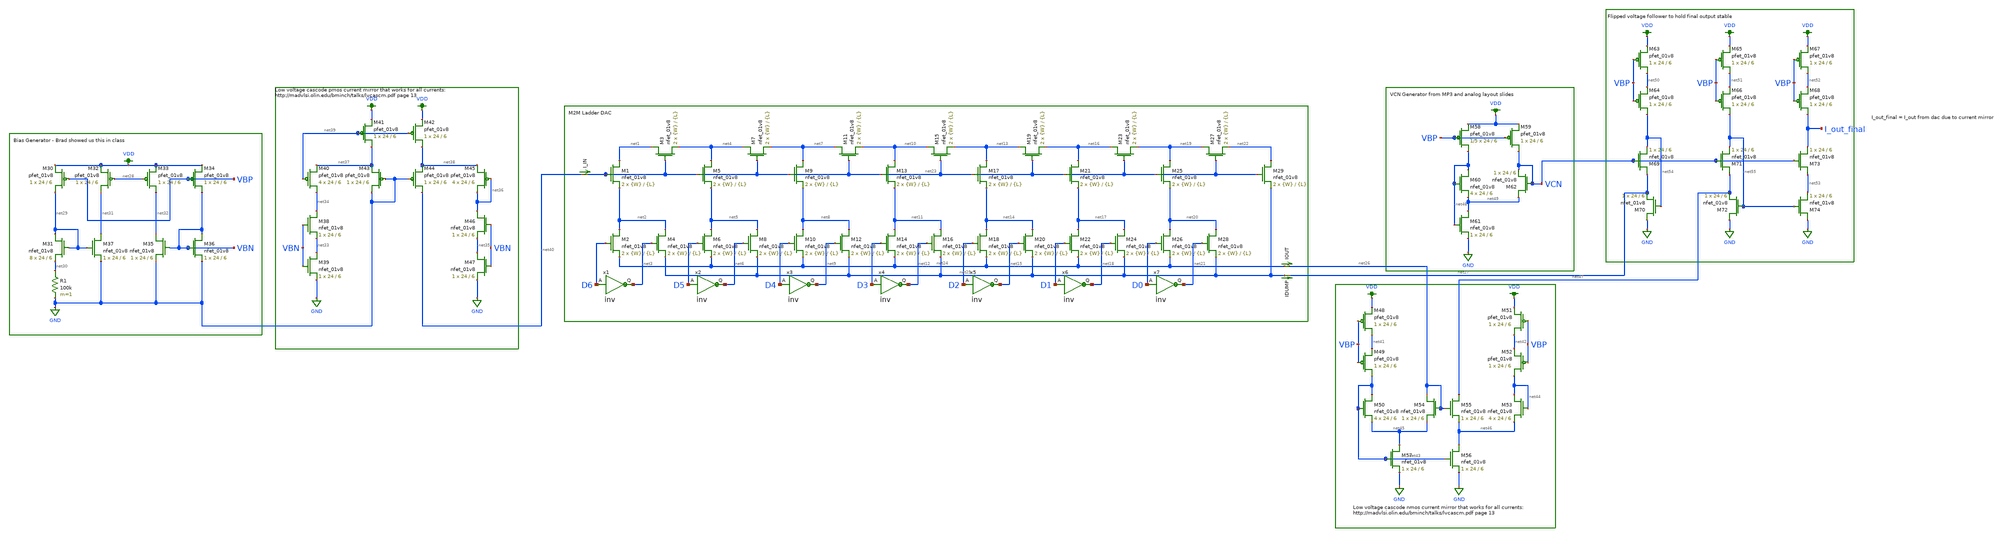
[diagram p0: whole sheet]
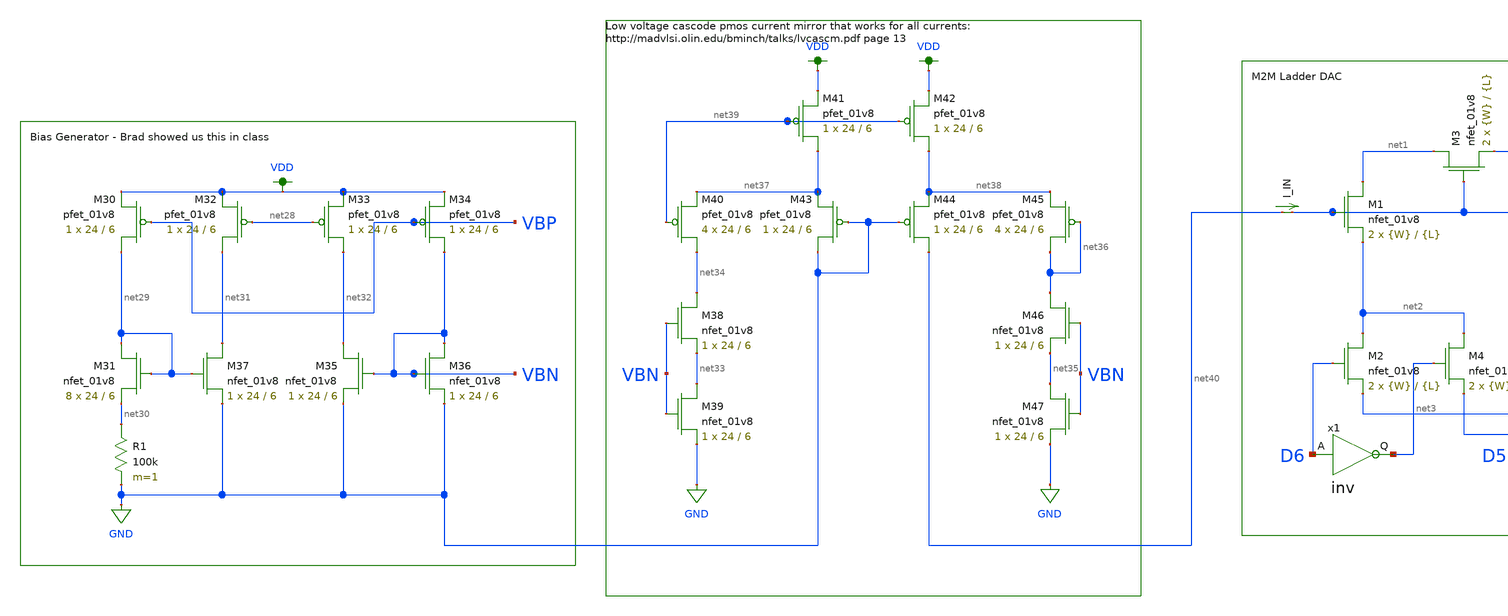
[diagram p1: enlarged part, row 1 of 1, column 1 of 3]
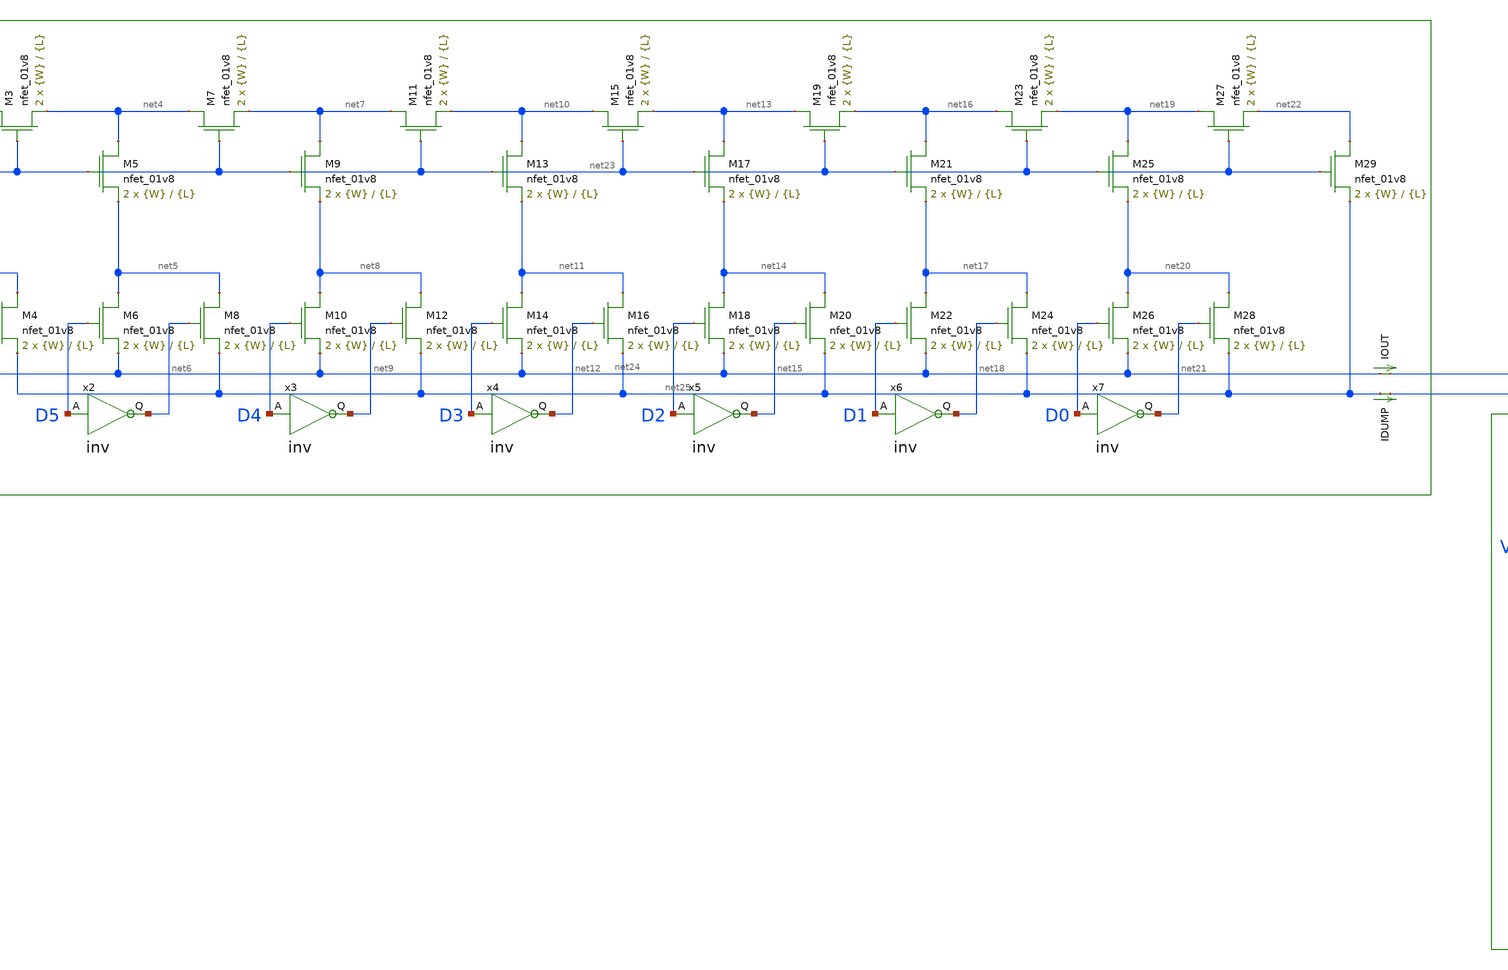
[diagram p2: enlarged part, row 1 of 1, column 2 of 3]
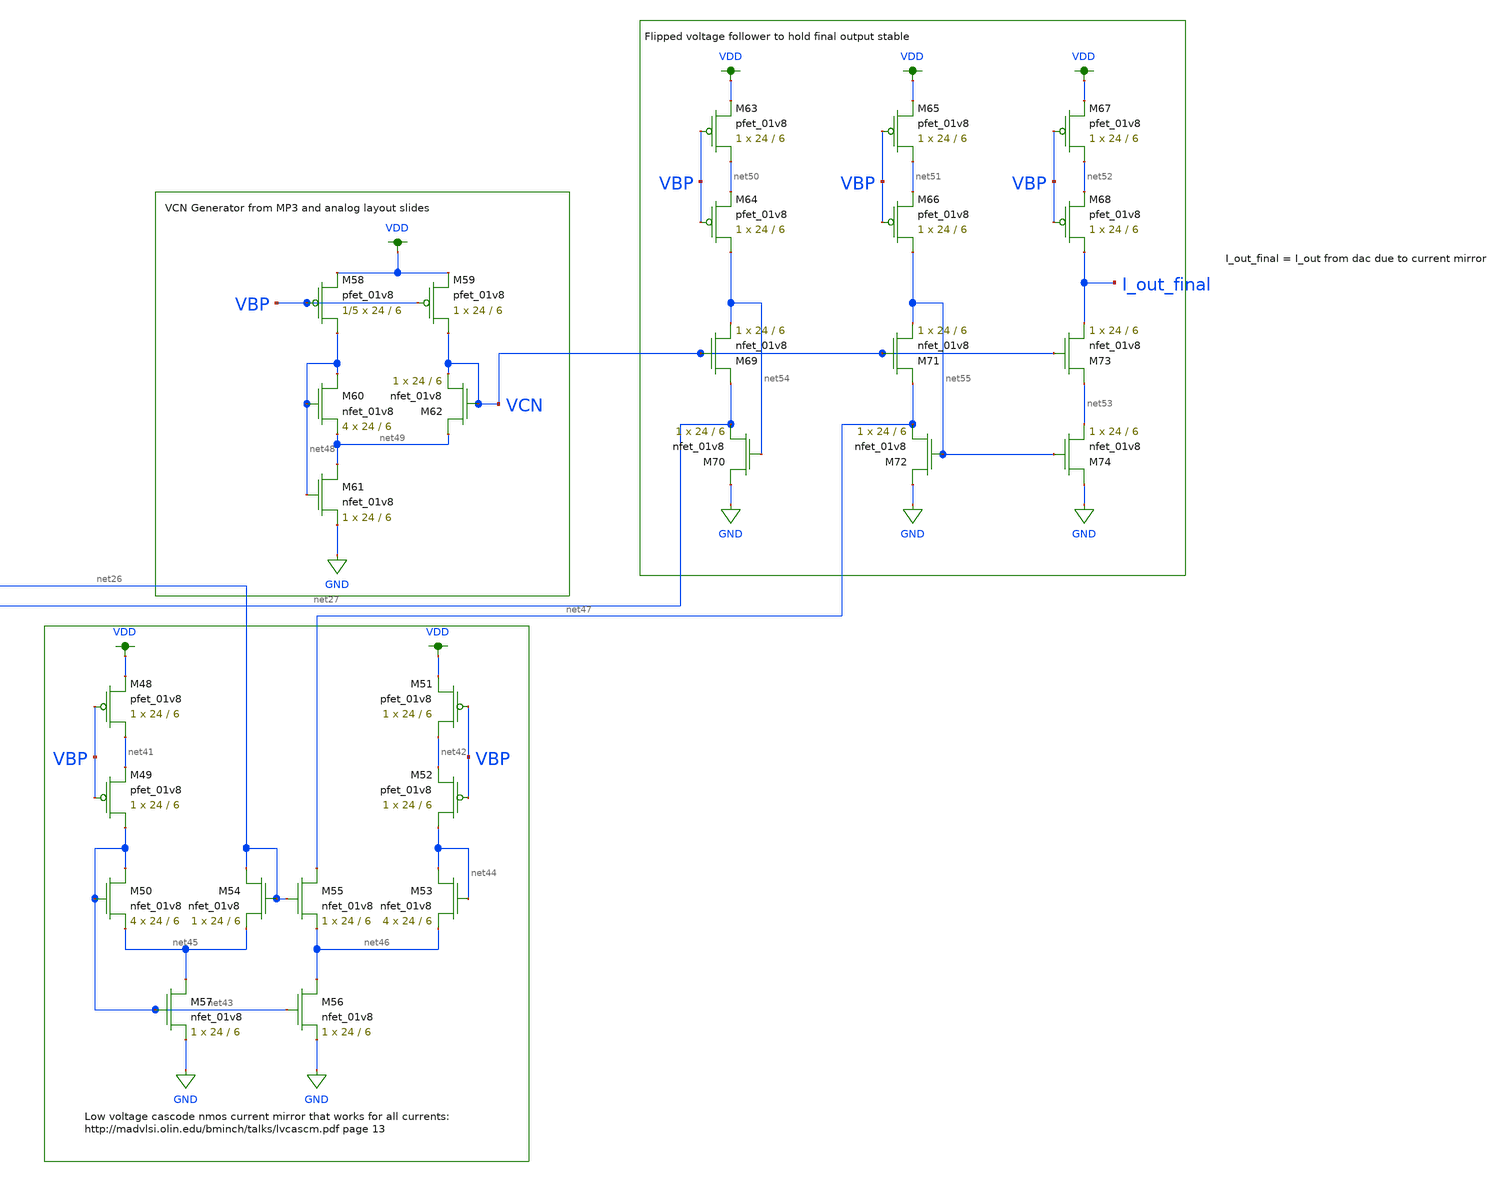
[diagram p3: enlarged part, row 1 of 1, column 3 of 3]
** sch_path: top_dac7.sch
**.subckt top_dac7
XM1 net1 net23 net2 GND sky130_fd_pr__nfet_01v8 L={L} W={W} nf=1 ad='int((nf+1)/2) * W/nf * 0.29' as='int((nf+2)/2) * W/nf * 0.29'
+ pd='2*int((nf+1)/2) * (W/nf + 0.29)' ps='2*int((nf+2)/2) * (W/nf + 0.29)' nrd='0.29 / W' nrs='0.29 / W'
+ sa=0 sb=0 sd=0 mult=2 m=2
IOUT net24 net26 0
.save i(iout)
XM2 net2 D6 net24 GND sky130_fd_pr__nfet_01v8 L={L} W={W} nf=1 ad='int((nf+1)/2) * W/nf * 0.29' as='int((nf+2)/2) * W/nf * 0.29'
+ pd='2*int((nf+1)/2) * (W/nf + 0.29)' ps='2*int((nf+2)/2) * (W/nf + 0.29)' nrd='0.29 / W' nrs='0.29 / W'
+ sa=0 sb=0 sd=0 mult=2 m=2
XM3 net1 net23 net4 GND sky130_fd_pr__nfet_01v8 L={L} W={W} nf=1 ad='int((nf+1)/2) * W/nf * 0.29' as='int((nf+2)/2) * W/nf * 0.29'
+ pd='2*int((nf+1)/2) * (W/nf + 0.29)' ps='2*int((nf+2)/2) * (W/nf + 0.29)' nrd='0.29 / W' nrs='0.29 / W'
+ sa=0 sb=0 sd=0 mult=2 m=2
XM4 net2 net3 net25 GND sky130_fd_pr__nfet_01v8 L={L} W={W} nf=1 ad='int((nf+1)/2) * W/nf * 0.29' as='int((nf+2)/2) * W/nf * 0.29'
+ pd='2*int((nf+1)/2) * (W/nf + 0.29)' ps='2*int((nf+2)/2) * (W/nf + 0.29)' nrd='0.29 / W' nrs='0.29 / W'
+ sa=0 sb=0 sd=0 mult=2 m=2
XM5 net4 net23 net5 GND sky130_fd_pr__nfet_01v8 L={L} W={W} nf=1 ad='int((nf+1)/2) * W/nf * 0.29' as='int((nf+2)/2) * W/nf * 0.29'
+ pd='2*int((nf+1)/2) * (W/nf + 0.29)' ps='2*int((nf+2)/2) * (W/nf + 0.29)' nrd='0.29 / W' nrs='0.29 / W'
+ sa=0 sb=0 sd=0 mult=2 m=2
XM6 net5 D5 net24 GND sky130_fd_pr__nfet_01v8 L={L} W={W} nf=1 ad='int((nf+1)/2) * W/nf * 0.29' as='int((nf+2)/2) * W/nf * 0.29'
+ pd='2*int((nf+1)/2) * (W/nf + 0.29)' ps='2*int((nf+2)/2) * (W/nf + 0.29)' nrd='0.29 / W' nrs='0.29 / W'
+ sa=0 sb=0 sd=0 mult=2 m=2
XM7 net4 net23 net7 GND sky130_fd_pr__nfet_01v8 L={L} W={W} nf=1 ad='int((nf+1)/2) * W/nf * 0.29' as='int((nf+2)/2) * W/nf * 0.29'
+ pd='2*int((nf+1)/2) * (W/nf + 0.29)' ps='2*int((nf+2)/2) * (W/nf + 0.29)' nrd='0.29 / W' nrs='0.29 / W'
+ sa=0 sb=0 sd=0 mult=2 m=2
XM8 net5 net6 net25 GND sky130_fd_pr__nfet_01v8 L={L} W={W} nf=1 ad='int((nf+1)/2) * W/nf * 0.29' as='int((nf+2)/2) * W/nf * 0.29'
+ pd='2*int((nf+1)/2) * (W/nf + 0.29)' ps='2*int((nf+2)/2) * (W/nf + 0.29)' nrd='0.29 / W' nrs='0.29 / W'
+ sa=0 sb=0 sd=0 mult=2 m=2
XM9 net7 net23 net8 GND sky130_fd_pr__nfet_01v8 L={L} W={W} nf=1 ad='int((nf+1)/2) * W/nf * 0.29' as='int((nf+2)/2) * W/nf * 0.29'
+ pd='2*int((nf+1)/2) * (W/nf + 0.29)' ps='2*int((nf+2)/2) * (W/nf + 0.29)' nrd='0.29 / W' nrs='0.29 / W'
+ sa=0 sb=0 sd=0 mult=2 m=2
XM10 net8 D4 net24 GND sky130_fd_pr__nfet_01v8 L={L} W={W} nf=1 ad='int((nf+1)/2) * W/nf * 0.29' as='int((nf+2)/2) * W/nf * 0.29'
+ pd='2*int((nf+1)/2) * (W/nf + 0.29)' ps='2*int((nf+2)/2) * (W/nf + 0.29)' nrd='0.29 / W' nrs='0.29 / W'
+ sa=0 sb=0 sd=0 mult=2 m=2
XM11 net7 net23 net10 GND sky130_fd_pr__nfet_01v8 L={L} W={W} nf=1 ad='int((nf+1)/2) * W/nf * 0.29' as='int((nf+2)/2) * W/nf * 0.29'
+ pd='2*int((nf+1)/2) * (W/nf + 0.29)' ps='2*int((nf+2)/2) * (W/nf + 0.29)' nrd='0.29 / W' nrs='0.29 / W'
+ sa=0 sb=0 sd=0 mult=2 m=2
XM12 net8 net9 net25 GND sky130_fd_pr__nfet_01v8 L={L} W={W} nf=1 ad='int((nf+1)/2) * W/nf * 0.29' as='int((nf+2)/2) * W/nf * 0.29'
+ pd='2*int((nf+1)/2) * (W/nf + 0.29)' ps='2*int((nf+2)/2) * (W/nf + 0.29)' nrd='0.29 / W' nrs='0.29 / W'
+ sa=0 sb=0 sd=0 mult=2 m=2
XM13 net10 net23 net11 GND sky130_fd_pr__nfet_01v8 L={L} W={W} nf=1 ad='int((nf+1)/2) * W/nf * 0.29'
+ as='int((nf+2)/2) * W/nf * 0.29' pd='2*int((nf+1)/2) * (W/nf + 0.29)' ps='2*int((nf+2)/2) * (W/nf + 0.29)'
+ nrd='0.29 / W' nrs='0.29 / W' sa=0 sb=0 sd=0 mult=2 m=2
XM14 net11 D3 net24 GND sky130_fd_pr__nfet_01v8 L={L} W={W} nf=1 ad='int((nf+1)/2) * W/nf * 0.29' as='int((nf+2)/2) * W/nf * 0.29'
+ pd='2*int((nf+1)/2) * (W/nf + 0.29)' ps='2*int((nf+2)/2) * (W/nf + 0.29)' nrd='0.29 / W' nrs='0.29 / W'
+ sa=0 sb=0 sd=0 mult=2 m=2
XM15 net10 net23 net13 GND sky130_fd_pr__nfet_01v8 L={L} W={W} nf=1 ad='int((nf+1)/2) * W/nf * 0.29'
+ as='int((nf+2)/2) * W/nf * 0.29' pd='2*int((nf+1)/2) * (W/nf + 0.29)' ps='2*int((nf+2)/2) * (W/nf + 0.29)'
+ nrd='0.29 / W' nrs='0.29 / W' sa=0 sb=0 sd=0 mult=2 m=2
XM16 net11 net12 net25 GND sky130_fd_pr__nfet_01v8 L={L} W={W} nf=1 ad='int((nf+1)/2) * W/nf * 0.29'
+ as='int((nf+2)/2) * W/nf * 0.29' pd='2*int((nf+1)/2) * (W/nf + 0.29)' ps='2*int((nf+2)/2) * (W/nf + 0.29)'
+ nrd='0.29 / W' nrs='0.29 / W' sa=0 sb=0 sd=0 mult=2 m=2
XM17 net13 net23 net14 GND sky130_fd_pr__nfet_01v8 L={L} W={W} nf=1 ad='int((nf+1)/2) * W/nf * 0.29'
+ as='int((nf+2)/2) * W/nf * 0.29' pd='2*int((nf+1)/2) * (W/nf + 0.29)' ps='2*int((nf+2)/2) * (W/nf + 0.29)'
+ nrd='0.29 / W' nrs='0.29 / W' sa=0 sb=0 sd=0 mult=2 m=2
XM18 net14 D2 net24 GND sky130_fd_pr__nfet_01v8 L={L} W={W} nf=1 ad='int((nf+1)/2) * W/nf * 0.29' as='int((nf+2)/2) * W/nf * 0.29'
+ pd='2*int((nf+1)/2) * (W/nf + 0.29)' ps='2*int((nf+2)/2) * (W/nf + 0.29)' nrd='0.29 / W' nrs='0.29 / W'
+ sa=0 sb=0 sd=0 mult=2 m=2
XM19 net13 net23 net16 GND sky130_fd_pr__nfet_01v8 L={L} W={W} nf=1 ad='int((nf+1)/2) * W/nf * 0.29'
+ as='int((nf+2)/2) * W/nf * 0.29' pd='2*int((nf+1)/2) * (W/nf + 0.29)' ps='2*int((nf+2)/2) * (W/nf + 0.29)'
+ nrd='0.29 / W' nrs='0.29 / W' sa=0 sb=0 sd=0 mult=2 m=2
XM20 net14 net15 net25 GND sky130_fd_pr__nfet_01v8 L={L} W={W} nf=1 ad='int((nf+1)/2) * W/nf * 0.29'
+ as='int((nf+2)/2) * W/nf * 0.29' pd='2*int((nf+1)/2) * (W/nf + 0.29)' ps='2*int((nf+2)/2) * (W/nf + 0.29)'
+ nrd='0.29 / W' nrs='0.29 / W' sa=0 sb=0 sd=0 mult=2 m=2
XM21 net16 net23 net17 GND sky130_fd_pr__nfet_01v8 L={L} W={W} nf=1 ad='int((nf+1)/2) * W/nf * 0.29'
+ as='int((nf+2)/2) * W/nf * 0.29' pd='2*int((nf+1)/2) * (W/nf + 0.29)' ps='2*int((nf+2)/2) * (W/nf + 0.29)'
+ nrd='0.29 / W' nrs='0.29 / W' sa=0 sb=0 sd=0 mult=2 m=2
XM22 net17 D1 net24 GND sky130_fd_pr__nfet_01v8 L={L} W={W} nf=1 ad='int((nf+1)/2) * W/nf * 0.29' as='int((nf+2)/2) * W/nf * 0.29'
+ pd='2*int((nf+1)/2) * (W/nf + 0.29)' ps='2*int((nf+2)/2) * (W/nf + 0.29)' nrd='0.29 / W' nrs='0.29 / W'
+ sa=0 sb=0 sd=0 mult=2 m=2
XM23 net16 net23 net19 GND sky130_fd_pr__nfet_01v8 L={L} W={W} nf=1 ad='int((nf+1)/2) * W/nf * 0.29'
+ as='int((nf+2)/2) * W/nf * 0.29' pd='2*int((nf+1)/2) * (W/nf + 0.29)' ps='2*int((nf+2)/2) * (W/nf + 0.29)'
+ nrd='0.29 / W' nrs='0.29 / W' sa=0 sb=0 sd=0 mult=2 m=2
XM24 net17 net18 net25 GND sky130_fd_pr__nfet_01v8 L={L} W={W} nf=1 ad='int((nf+1)/2) * W/nf * 0.29'
+ as='int((nf+2)/2) * W/nf * 0.29' pd='2*int((nf+1)/2) * (W/nf + 0.29)' ps='2*int((nf+2)/2) * (W/nf + 0.29)'
+ nrd='0.29 / W' nrs='0.29 / W' sa=0 sb=0 sd=0 mult=2 m=2
XM25 net19 net23 net20 GND sky130_fd_pr__nfet_01v8 L={L} W={W} nf=1 ad='int((nf+1)/2) * W/nf * 0.29'
+ as='int((nf+2)/2) * W/nf * 0.29' pd='2*int((nf+1)/2) * (W/nf + 0.29)' ps='2*int((nf+2)/2) * (W/nf + 0.29)'
+ nrd='0.29 / W' nrs='0.29 / W' sa=0 sb=0 sd=0 mult=2 m=2
XM26 net20 D0 net24 GND sky130_fd_pr__nfet_01v8 L={L} W={W} nf=1 ad='int((nf+1)/2) * W/nf * 0.29' as='int((nf+2)/2) * W/nf * 0.29'
+ pd='2*int((nf+1)/2) * (W/nf + 0.29)' ps='2*int((nf+2)/2) * (W/nf + 0.29)' nrd='0.29 / W' nrs='0.29 / W'
+ sa=0 sb=0 sd=0 mult=2 m=2
XM27 net19 net23 net22 GND sky130_fd_pr__nfet_01v8 L={L} W={W} nf=1 ad='int((nf+1)/2) * W/nf * 0.29'
+ as='int((nf+2)/2) * W/nf * 0.29' pd='2*int((nf+1)/2) * (W/nf + 0.29)' ps='2*int((nf+2)/2) * (W/nf + 0.29)'
+ nrd='0.29 / W' nrs='0.29 / W' sa=0 sb=0 sd=0 mult=2 m=2
XM28 net20 net21 net25 GND sky130_fd_pr__nfet_01v8 L={L} W={W} nf=1 ad='int((nf+1)/2) * W/nf * 0.29'
+ as='int((nf+2)/2) * W/nf * 0.29' pd='2*int((nf+1)/2) * (W/nf + 0.29)' ps='2*int((nf+2)/2) * (W/nf + 0.29)'
+ nrd='0.29 / W' nrs='0.29 / W' sa=0 sb=0 sd=0 mult=2 m=2
XM29 net22 net23 net25 GND sky130_fd_pr__nfet_01v8 L={L} W={W} nf=1 ad='int((nf+1)/2) * W/nf * 0.29'
+ as='int((nf+2)/2) * W/nf * 0.29' pd='2*int((nf+1)/2) * (W/nf + 0.29)' ps='2*int((nf+2)/2) * (W/nf + 0.29)'
+ nrd='0.29 / W' nrs='0.29 / W' sa=0 sb=0 sd=0 mult=2 m=2
IDUMP net25 net27 0
.save i(idump)
I_IN net40 net23 0
.save i(i_in)
x1 net3 D6 inv
x2 net6 D5 inv
x3 net9 D4 inv
x4 net12 D3 inv
x5 net15 D2 inv
x6 net18 D1 inv
x7 net21 D0 inv
XM30 net29 VBP VDD VDD sky130_fd_pr__pfet_01v8 L=6 W=24 nf=1 ad='int((nf+1)/2) * W/nf * 0.29' as='int((nf+2)/2) * W/nf * 0.29'
+ pd='2*int((nf+1)/2) * (W/nf + 0.29)' ps='2*int((nf+2)/2) * (W/nf + 0.29)' nrd='0.29 / W' nrs='0.29 / W'
+ sa=0 sb=0 sd=0 mult=1 m=1
XM31 net29 net29 net30 GND sky130_fd_pr__nfet_01v8 L=6 W=24 nf=1 ad='int((nf+1)/2) * W/nf * 0.29' as='int((nf+2)/2) * W/nf * 0.29'
+ pd='2*int((nf+1)/2) * (W/nf + 0.29)' ps='2*int((nf+2)/2) * (W/nf + 0.29)' nrd='0.29 / W' nrs='0.29 / W'
+ sa=0 sb=0 sd=0 mult=8 m=8
XM32 net31 net28 VDD VDD sky130_fd_pr__pfet_01v8 L=6 W=24 nf=1 ad='int((nf+1)/2) * W/nf * 0.29' as='int((nf+2)/2) * W/nf * 0.29'
+ pd='2*int((nf+1)/2) * (W/nf + 0.29)' ps='2*int((nf+2)/2) * (W/nf + 0.29)' nrd='0.29 / W' nrs='0.29 / W'
+ sa=0 sb=0 sd=0 mult=1 m=1
XM33 net32 net28 VDD VDD sky130_fd_pr__pfet_01v8 L=6 W=24 nf=1 ad='int((nf+1)/2) * W/nf * 0.29' as='int((nf+2)/2) * W/nf * 0.29'
+ pd='2*int((nf+1)/2) * (W/nf + 0.29)' ps='2*int((nf+2)/2) * (W/nf + 0.29)' nrd='0.29 / W' nrs='0.29 / W'
+ sa=0 sb=0 sd=0 mult=1 m=1
XM34 VBN VBP VDD VDD sky130_fd_pr__pfet_01v8 L=6 W=24 nf=1 ad='int((nf+1)/2) * W/nf * 0.29' as='int((nf+2)/2) * W/nf * 0.29'
+ pd='2*int((nf+1)/2) * (W/nf + 0.29)' ps='2*int((nf+2)/2) * (W/nf + 0.29)' nrd='0.29 / W' nrs='0.29 / W'
+ sa=0 sb=0 sd=0 mult=1 m=1
XM35 net32 VBN GND GND sky130_fd_pr__nfet_01v8 L=6 W=24 nf=1 ad='int((nf+1)/2) * W/nf * 0.29' as='int((nf+2)/2) * W/nf * 0.29'
+ pd='2*int((nf+1)/2) * (W/nf + 0.29)' ps='2*int((nf+2)/2) * (W/nf + 0.29)' nrd='0.29 / W' nrs='0.29 / W'
+ sa=0 sb=0 sd=0 mult=1 m=1
XM36 VBN VBN GND GND sky130_fd_pr__nfet_01v8 L=6 W=24 nf=1 ad='int((nf+1)/2) * W/nf * 0.29' as='int((nf+2)/2) * W/nf * 0.29'
+ pd='2*int((nf+1)/2) * (W/nf + 0.29)' ps='2*int((nf+2)/2) * (W/nf + 0.29)' nrd='0.29 / W' nrs='0.29 / W'
+ sa=0 sb=0 sd=0 mult=1 m=1
XM37 net31 net29 GND GND sky130_fd_pr__nfet_01v8 L=6 W=24 nf=1 ad='int((nf+1)/2) * W/nf * 0.29' as='int((nf+2)/2) * W/nf * 0.29'
+ pd='2*int((nf+1)/2) * (W/nf + 0.29)' ps='2*int((nf+2)/2) * (W/nf + 0.29)' nrd='0.29 / W' nrs='0.29 / W'
+ sa=0 sb=0 sd=0 mult=1 m=1
R1 net30 GND 100k m=1
XM38 net34 VBN net33 GND sky130_fd_pr__nfet_01v8 L=6 W=24 nf=1 ad='int((nf+1)/2) * W/nf * 0.29' as='int((nf+2)/2) * W/nf * 0.29'
+ pd='2*int((nf+1)/2) * (W/nf + 0.29)' ps='2*int((nf+2)/2) * (W/nf + 0.29)' nrd='0.29 / W' nrs='0.29 / W'
+ sa=0 sb=0 sd=0 mult=1 m=1
XM39 net33 VBN GND GND sky130_fd_pr__nfet_01v8 L=6 W=24 nf=1 ad='int((nf+1)/2) * W/nf * 0.29' as='int((nf+2)/2) * W/nf * 0.29'
+ pd='2*int((nf+1)/2) * (W/nf + 0.29)' ps='2*int((nf+2)/2) * (W/nf + 0.29)' nrd='0.29 / W' nrs='0.29 / W'
+ sa=0 sb=0 sd=0 mult=1 m=1
XM40 net34 net39 net37 VDD sky130_fd_pr__pfet_01v8 L=6 W=24 nf=1 ad='int((nf+1)/2) * W/nf * 0.29' as='int((nf+2)/2) * W/nf * 0.29'
+ pd='2*int((nf+1)/2) * (W/nf + 0.29)' ps='2*int((nf+2)/2) * (W/nf + 0.29)' nrd='0.29 / W' nrs='0.29 / W'
+ sa=0 sb=0 sd=0 mult=4 m=4
XM41 net37 net39 VDD VDD sky130_fd_pr__pfet_01v8 L=6 W=24 nf=1 ad='int((nf+1)/2) * W/nf * 0.29' as='int((nf+2)/2) * W/nf * 0.29'
+ pd='2*int((nf+1)/2) * (W/nf + 0.29)' ps='2*int((nf+2)/2) * (W/nf + 0.29)' nrd='0.29 / W' nrs='0.29 / W'
+ sa=0 sb=0 sd=0 mult=1 m=1
XM42 net38 net39 VDD VDD sky130_fd_pr__pfet_01v8 L=6 W=24 nf=1 ad='int((nf+1)/2) * W/nf * 0.29' as='int((nf+2)/2) * W/nf * 0.29'
+ pd='2*int((nf+1)/2) * (W/nf + 0.29)' ps='2*int((nf+2)/2) * (W/nf + 0.29)' nrd='0.29 / W' nrs='0.29 / W'
+ sa=0 sb=0 sd=0 mult=1 m=1
XM43 GND GND net37 VDD sky130_fd_pr__pfet_01v8 L=6 W=24 nf=1 ad='int((nf+1)/2) * W/nf * 0.29' as='int((nf+2)/2) * W/nf * 0.29'
+ pd='2*int((nf+1)/2) * (W/nf + 0.29)' ps='2*int((nf+2)/2) * (W/nf + 0.29)' nrd='0.29 / W' nrs='0.29 / W'
+ sa=0 sb=0 sd=0 mult=1 m=1
XM44 net40 GND net38 VDD sky130_fd_pr__pfet_01v8 L=6 W=24 nf=1 ad='int((nf+1)/2) * W/nf * 0.29' as='int((nf+2)/2) * W/nf * 0.29'
+ pd='2*int((nf+1)/2) * (W/nf + 0.29)' ps='2*int((nf+2)/2) * (W/nf + 0.29)' nrd='0.29 / W' nrs='0.29 / W'
+ sa=0 sb=0 sd=0 mult=1 m=1
XM45 net36 net36 net38 VDD sky130_fd_pr__pfet_01v8 L=6 W=24 nf=1 ad='int((nf+1)/2) * W/nf * 0.29' as='int((nf+2)/2) * W/nf * 0.29'
+ pd='2*int((nf+1)/2) * (W/nf + 0.29)' ps='2*int((nf+2)/2) * (W/nf + 0.29)' nrd='0.29 / W' nrs='0.29 / W'
+ sa=0 sb=0 sd=0 mult=4 m=4
XM46 net36 VBN net35 GND sky130_fd_pr__nfet_01v8 L=6 W=24 nf=1 ad='int((nf+1)/2) * W/nf * 0.29' as='int((nf+2)/2) * W/nf * 0.29'
+ pd='2*int((nf+1)/2) * (W/nf + 0.29)' ps='2*int((nf+2)/2) * (W/nf + 0.29)' nrd='0.29 / W' nrs='0.29 / W'
+ sa=0 sb=0 sd=0 mult=1 m=1
XM47 net35 VBN GND GND sky130_fd_pr__nfet_01v8 L=6 W=24 nf=1 ad='int((nf+1)/2) * W/nf * 0.29' as='int((nf+2)/2) * W/nf * 0.29'
+ pd='2*int((nf+1)/2) * (W/nf + 0.29)' ps='2*int((nf+2)/2) * (W/nf + 0.29)' nrd='0.29 / W' nrs='0.29 / W'
+ sa=0 sb=0 sd=0 mult=1 m=1
XM48 net41 VBP VDD VDD sky130_fd_pr__pfet_01v8 L=6 W=24 nf=1 ad='int((nf+1)/2) * W/nf * 0.29' as='int((nf+2)/2) * W/nf * 0.29'
+ pd='2*int((nf+1)/2) * (W/nf + 0.29)' ps='2*int((nf+2)/2) * (W/nf + 0.29)' nrd='0.29 / W' nrs='0.29 / W'
+ sa=0 sb=0 sd=0 mult=1 m=1
XM49 net43 VBP net41 VDD sky130_fd_pr__pfet_01v8 L=6 W=24 nf=1 ad='int((nf+1)/2) * W/nf * 0.29' as='int((nf+2)/2) * W/nf * 0.29'
+ pd='2*int((nf+1)/2) * (W/nf + 0.29)' ps='2*int((nf+2)/2) * (W/nf + 0.29)' nrd='0.29 / W' nrs='0.29 / W'
+ sa=0 sb=0 sd=0 mult=1 m=1
XM50 net43 net43 net45 GND sky130_fd_pr__nfet_01v8 L=6 W=24 nf=1 ad='int((nf+1)/2) * W/nf * 0.29' as='int((nf+2)/2) * W/nf * 0.29'
+ pd='2*int((nf+1)/2) * (W/nf + 0.29)' ps='2*int((nf+2)/2) * (W/nf + 0.29)' nrd='0.29 / W' nrs='0.29 / W'
+ sa=0 sb=0 sd=0 mult=4 m=4
XM51 net42 VBP VDD VDD sky130_fd_pr__pfet_01v8 L=6 W=24 nf=1 ad='int((nf+1)/2) * W/nf * 0.29' as='int((nf+2)/2) * W/nf * 0.29'
+ pd='2*int((nf+1)/2) * (W/nf + 0.29)' ps='2*int((nf+2)/2) * (W/nf + 0.29)' nrd='0.29 / W' nrs='0.29 / W'
+ sa=0 sb=0 sd=0 mult=1 m=1
XM52 net44 VBP net42 VDD sky130_fd_pr__pfet_01v8 L=6 W=24 nf=1 ad='int((nf+1)/2) * W/nf * 0.29' as='int((nf+2)/2) * W/nf * 0.29'
+ pd='2*int((nf+1)/2) * (W/nf + 0.29)' ps='2*int((nf+2)/2) * (W/nf + 0.29)' nrd='0.29 / W' nrs='0.29 / W'
+ sa=0 sb=0 sd=0 mult=1 m=1
XM53 net44 net44 net46 GND sky130_fd_pr__nfet_01v8 L=6 W=24 nf=1 ad='int((nf+1)/2) * W/nf * 0.29' as='int((nf+2)/2) * W/nf * 0.29'
+ pd='2*int((nf+1)/2) * (W/nf + 0.29)' ps='2*int((nf+2)/2) * (W/nf + 0.29)' nrd='0.29 / W' nrs='0.29 / W'
+ sa=0 sb=0 sd=0 mult=4 m=4
XM54 net26 net26 net45 GND sky130_fd_pr__nfet_01v8 L=6 W=24 nf=1 ad='int((nf+1)/2) * W/nf * 0.29' as='int((nf+2)/2) * W/nf * 0.29'
+ pd='2*int((nf+1)/2) * (W/nf + 0.29)' ps='2*int((nf+2)/2) * (W/nf + 0.29)' nrd='0.29 / W' nrs='0.29 / W'
+ sa=0 sb=0 sd=0 mult=1 m=1
XM55 net47 net26 net46 GND sky130_fd_pr__nfet_01v8 L=6 W=24 nf=1 ad='int((nf+1)/2) * W/nf * 0.29' as='int((nf+2)/2) * W/nf * 0.29'
+ pd='2*int((nf+1)/2) * (W/nf + 0.29)' ps='2*int((nf+2)/2) * (W/nf + 0.29)' nrd='0.29 / W' nrs='0.29 / W'
+ sa=0 sb=0 sd=0 mult=1 m=1
XM56 net46 net43 GND GND sky130_fd_pr__nfet_01v8 L=6 W=24 nf=1 ad='int((nf+1)/2) * W/nf * 0.29' as='int((nf+2)/2) * W/nf * 0.29'
+ pd='2*int((nf+1)/2) * (W/nf + 0.29)' ps='2*int((nf+2)/2) * (W/nf + 0.29)' nrd='0.29 / W' nrs='0.29 / W'
+ sa=0 sb=0 sd=0 mult=1 m=1
XM57 net45 net43 GND GND sky130_fd_pr__nfet_01v8 L=6 W=24 nf=1 ad='int((nf+1)/2) * W/nf * 0.29' as='int((nf+2)/2) * W/nf * 0.29'
+ pd='2*int((nf+1)/2) * (W/nf + 0.29)' ps='2*int((nf+2)/2) * (W/nf + 0.29)' nrd='0.29 / W' nrs='0.29 / W'
+ sa=0 sb=0 sd=0 mult=1 m=1
XM58 net48 VBP VDD VDD sky130_fd_pr__pfet_01v8 L=6 W=24 nf=1 ad='int((nf+1)/2) * W/nf * 0.29' as='int((nf+2)/2) * W/nf * 0.29'
+ pd='2*int((nf+1)/2) * (W/nf + 0.29)' ps='2*int((nf+2)/2) * (W/nf + 0.29)' nrd='0.29 / W' nrs='0.29 / W'
+ sa=0 sb=0 sd=0 mult=1/5 m=1/5
XM59 VCN VBP VDD VDD sky130_fd_pr__pfet_01v8 L=6 W=24 nf=1 ad='int((nf+1)/2) * W/nf * 0.29' as='int((nf+2)/2) * W/nf * 0.29'
+ pd='2*int((nf+1)/2) * (W/nf + 0.29)' ps='2*int((nf+2)/2) * (W/nf + 0.29)' nrd='0.29 / W' nrs='0.29 / W'
+ sa=0 sb=0 sd=0 mult=1 m=1
XM60 net48 net48 net49 GND sky130_fd_pr__nfet_01v8 L=6 W=24 nf=1 ad='int((nf+1)/2) * W/nf * 0.29' as='int((nf+2)/2) * W/nf * 0.29'
+ pd='2*int((nf+1)/2) * (W/nf + 0.29)' ps='2*int((nf+2)/2) * (W/nf + 0.29)' nrd='0.29 / W' nrs='0.29 / W'
+ sa=0 sb=0 sd=0 mult=4 m=4
XM61 net49 net48 GND GND sky130_fd_pr__nfet_01v8 L=6 W=24 nf=1 ad='int((nf+1)/2) * W/nf * 0.29' as='int((nf+2)/2) * W/nf * 0.29'
+ pd='2*int((nf+1)/2) * (W/nf + 0.29)' ps='2*int((nf+2)/2) * (W/nf + 0.29)' nrd='0.29 / W' nrs='0.29 / W'
+ sa=0 sb=0 sd=0 mult=1 m=1
XM62 net49 VCN VCN GND sky130_fd_pr__nfet_01v8 L=6 W=24 nf=1 ad='int((nf+1)/2) * W/nf * 0.29' as='int((nf+2)/2) * W/nf * 0.29'
+ pd='2*int((nf+1)/2) * (W/nf + 0.29)' ps='2*int((nf+2)/2) * (W/nf + 0.29)' nrd='0.29 / W' nrs='0.29 / W'
+ sa=0 sb=0 sd=0 mult=1 m=1
XM63 net50 VBP VDD VDD sky130_fd_pr__pfet_01v8 L=6 W=24 nf=1 ad='int((nf+1)/2) * W/nf * 0.29' as='int((nf+2)/2) * W/nf * 0.29'
+ pd='2*int((nf+1)/2) * (W/nf + 0.29)' ps='2*int((nf+2)/2) * (W/nf + 0.29)' nrd='0.29 / W' nrs='0.29 / W'
+ sa=0 sb=0 sd=0 mult=1 m=1
XM64 net54 VBP net50 VDD sky130_fd_pr__pfet_01v8 L=6 W=24 nf=1 ad='int((nf+1)/2) * W/nf * 0.29' as='int((nf+2)/2) * W/nf * 0.29'
+ pd='2*int((nf+1)/2) * (W/nf + 0.29)' ps='2*int((nf+2)/2) * (W/nf + 0.29)' nrd='0.29 / W' nrs='0.29 / W'
+ sa=0 sb=0 sd=0 mult=1 m=1
XM65 net51 VBP VDD VDD sky130_fd_pr__pfet_01v8 L=6 W=24 nf=1 ad='int((nf+1)/2) * W/nf * 0.29' as='int((nf+2)/2) * W/nf * 0.29'
+ pd='2*int((nf+1)/2) * (W/nf + 0.29)' ps='2*int((nf+2)/2) * (W/nf + 0.29)' nrd='0.29 / W' nrs='0.29 / W'
+ sa=0 sb=0 sd=0 mult=1 m=1
XM66 net55 VBP net51 VDD sky130_fd_pr__pfet_01v8 L=6 W=24 nf=1 ad='int((nf+1)/2) * W/nf * 0.29' as='int((nf+2)/2) * W/nf * 0.29'
+ pd='2*int((nf+1)/2) * (W/nf + 0.29)' ps='2*int((nf+2)/2) * (W/nf + 0.29)' nrd='0.29 / W' nrs='0.29 / W'
+ sa=0 sb=0 sd=0 mult=1 m=1
XM67 net52 VBP VDD VDD sky130_fd_pr__pfet_01v8 L=6 W=24 nf=1 ad='int((nf+1)/2) * W/nf * 0.29' as='int((nf+2)/2) * W/nf * 0.29'
+ pd='2*int((nf+1)/2) * (W/nf + 0.29)' ps='2*int((nf+2)/2) * (W/nf + 0.29)' nrd='0.29 / W' nrs='0.29 / W'
+ sa=0 sb=0 sd=0 mult=1 m=1
XM68 I_out_final VBP net52 VDD sky130_fd_pr__pfet_01v8 L=6 W=24 nf=1 ad='int((nf+1)/2) * W/nf * 0.29'
+ as='int((nf+2)/2) * W/nf * 0.29' pd='2*int((nf+1)/2) * (W/nf + 0.29)' ps='2*int((nf+2)/2) * (W/nf + 0.29)'
+ nrd='0.29 / W' nrs='0.29 / W' sa=0 sb=0 sd=0 mult=1 m=1
XM69 net27 VCN net54 GND sky130_fd_pr__nfet_01v8 L=6 W=24 nf=1 ad='int((nf+1)/2) * W/nf * 0.29' as='int((nf+2)/2) * W/nf * 0.29'
+ pd='2*int((nf+1)/2) * (W/nf + 0.29)' ps='2*int((nf+2)/2) * (W/nf + 0.29)' nrd='0.29 / W' nrs='0.29 / W'
+ sa=0 sb=0 sd=0 mult=1 m=1
XM70 GND net54 net27 GND sky130_fd_pr__nfet_01v8 L=6 W=24 nf=1 ad='int((nf+1)/2) * W/nf * 0.29' as='int((nf+2)/2) * W/nf * 0.29'
+ pd='2*int((nf+1)/2) * (W/nf + 0.29)' ps='2*int((nf+2)/2) * (W/nf + 0.29)' nrd='0.29 / W' nrs='0.29 / W'
+ sa=0 sb=0 sd=0 mult=1 m=1
XM71 net47 VCN net55 GND sky130_fd_pr__nfet_01v8 L=6 W=24 nf=1 ad='int((nf+1)/2) * W/nf * 0.29' as='int((nf+2)/2) * W/nf * 0.29'
+ pd='2*int((nf+1)/2) * (W/nf + 0.29)' ps='2*int((nf+2)/2) * (W/nf + 0.29)' nrd='0.29 / W' nrs='0.29 / W'
+ sa=0 sb=0 sd=0 mult=1 m=1
XM72 GND net55 net47 GND sky130_fd_pr__nfet_01v8 L=6 W=24 nf=1 ad='int((nf+1)/2) * W/nf * 0.29' as='int((nf+2)/2) * W/nf * 0.29'
+ pd='2*int((nf+1)/2) * (W/nf + 0.29)' ps='2*int((nf+2)/2) * (W/nf + 0.29)' nrd='0.29 / W' nrs='0.29 / W'
+ sa=0 sb=0 sd=0 mult=1 m=1
XM73 net53 VCN I_out_final GND sky130_fd_pr__nfet_01v8 L=6 W=24 nf=1 ad='int((nf+1)/2) * W/nf * 0.29'
+ as='int((nf+2)/2) * W/nf * 0.29' pd='2*int((nf+1)/2) * (W/nf + 0.29)' ps='2*int((nf+2)/2) * (W/nf + 0.29)'
+ nrd='0.29 / W' nrs='0.29 / W' sa=0 sb=0 sd=0 mult=1 m=1
XM74 GND net55 net53 GND sky130_fd_pr__nfet_01v8 L=6 W=24 nf=1 ad='int((nf+1)/2) * W/nf * 0.29' as='int((nf+2)/2) * W/nf * 0.29'
+ pd='2*int((nf+1)/2) * (W/nf + 0.29)' ps='2*int((nf+2)/2) * (W/nf + 0.29)' nrd='0.29 / W' nrs='0.29 / W'
+ sa=0 sb=0 sd=0 mult=1 m=1
**.ends

* expanding   symbol:  /home/mstopyra/Documents/MADVLSI-MP4-DAC/schemas/inv.sym # of pins=2
** sym_path: /home/mstopyra/Documents/MADVLSI-MP4-DAC/schemas/inv.sym
** sch_path: /home/mstopyra/Documents/MADVLSI-MP4-DAC/schemas/inv.sch
.subckt inv Q A
*.ipin A
*.opin Q
XM1 Q A GND GND sky130_fd_pr__nfet_01v8 L=4 W=32 nf=1 ad='int((nf+1)/2) * W/nf * 0.29' as='int((nf+2)/2) * W/nf * 0.29'
+ pd='2*int((nf+1)/2) * (W/nf + 0.29)' ps='2*int((nf+2)/2) * (W/nf + 0.29)' nrd='0.29 / W' nrs='0.29 / W'
+ sa=0 sb=0 sd=0 mult=2 m=2
XM2 Q A VDD VDD sky130_fd_pr__pfet_01v8 L=4 W=32 nf=1 ad='int((nf+1)/2) * W/nf * 0.29' as='int((nf+2)/2) * W/nf * 0.29'
+ pd='2*int((nf+1)/2) * (W/nf + 0.29)' ps='2*int((nf+2)/2) * (W/nf + 0.29)' nrd='0.29 / W' nrs='0.29 / W'
+ sa=0 sb=0 sd=0 mult=1 m=1
.ends

.GLOBAL GND
.GLOBAL VDD
.end
